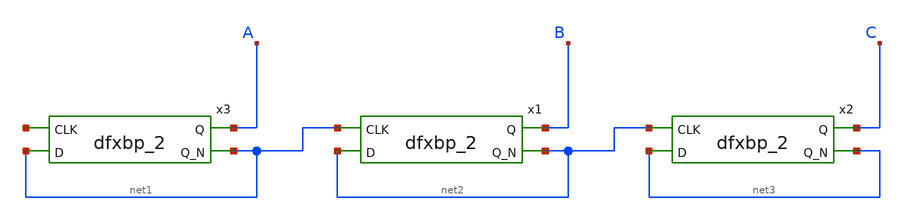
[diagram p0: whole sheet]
** sch_path: xschem/PLL_FOLDER/divider/untitled-9.sch
**.subckt untitled-9
x3 net4 net1 VSS VSS VDD VDD A net1 sky130_fd_sc_hd__dfxbp_2
x1 net1 net2 VSS VSS VDD VDD B net2 sky130_fd_sc_hd__dfxbp_2
x2 net2 net3 VSS VSS VDD VDD C net3 sky130_fd_sc_hd__dfxbp_2
**.ends
.end
